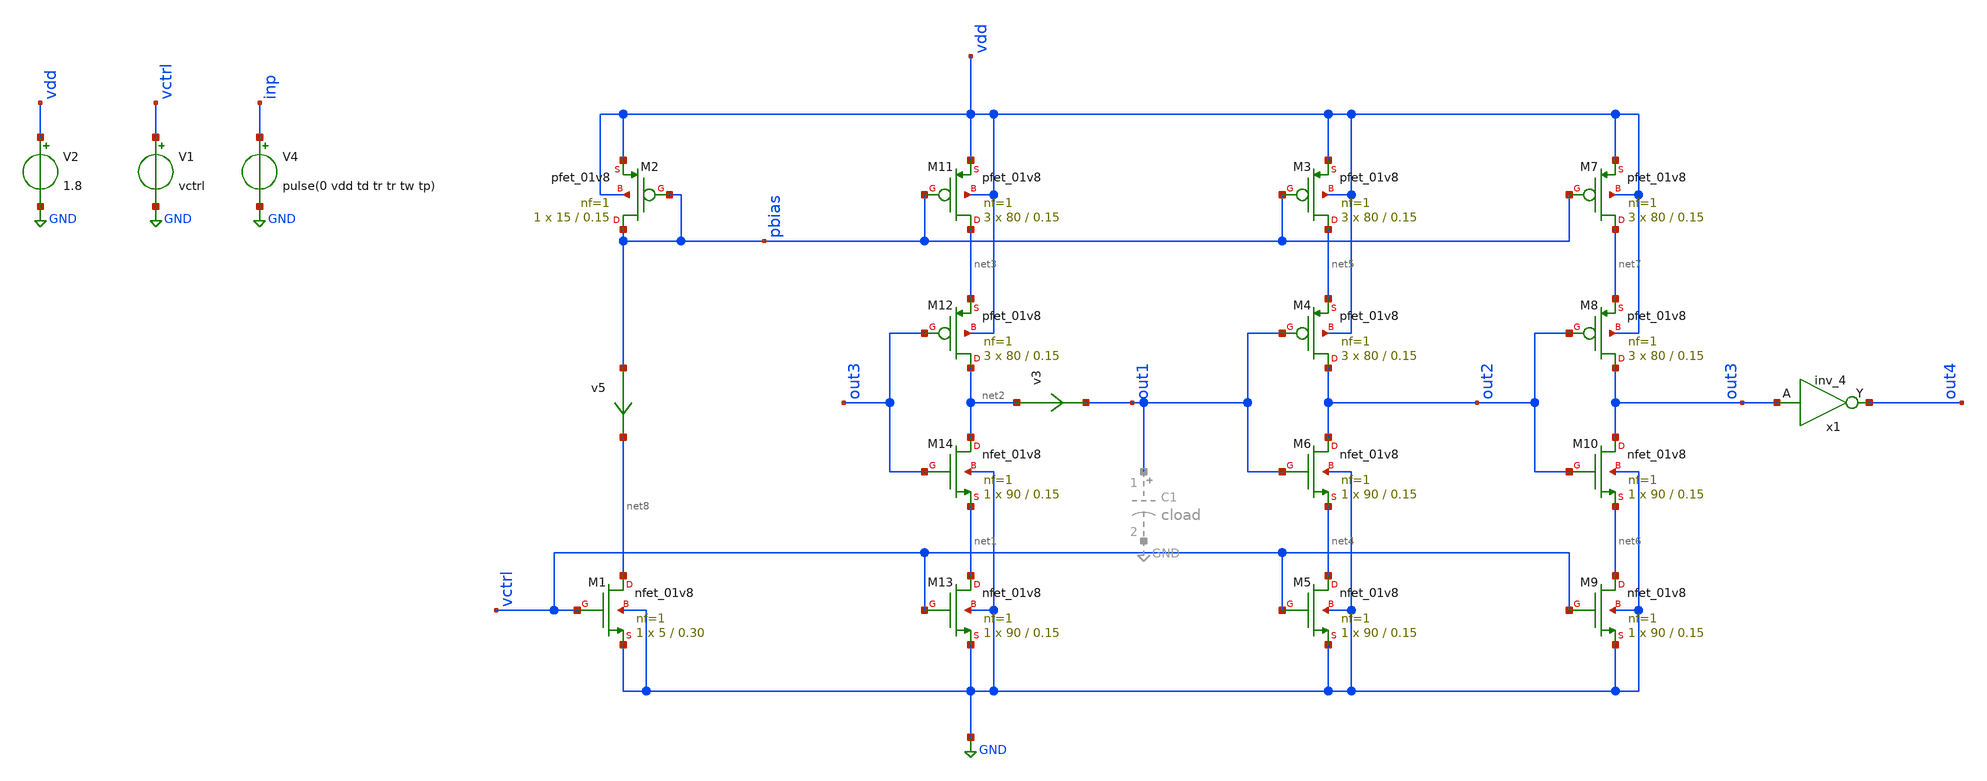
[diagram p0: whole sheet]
** sch_path: xschem/inv_delay.sch
**.subckt inv_delay
XM1 net8 vctrl GND GND sky130_fd_pr__nfet_01v8 L=0.30 W=5 nf=1 ad='int((nf+1)/2) * W/nf * 0.29' as='int((nf+2)/2) * W/nf * 0.29'
+ pd='2*int((nf+1)/2) * (W/nf + 0.29)' ps='2*int((nf+2)/2) * (W/nf + 0.29)' nrd='0.29 / W' nrs='0.29 / W'
+ sa=0 sb=0 sd=0 mult=1 m=1
XM2 pbias pbias vdd vdd sky130_fd_pr__pfet_01v8 L=0.15 W=15 nf=1 ad='int((nf+1)/2) * W/nf * 0.29' as='int((nf+2)/2) * W/nf * 0.29'
+ pd='2*int((nf+1)/2) * (W/nf + 0.29)' ps='2*int((nf+2)/2) * (W/nf + 0.29)' nrd='0.29 / W' nrs='0.29 / W'
+ sa=0 sb=0 sd=0 mult=1 m=1
XM11 net3 pbias vdd vdd sky130_fd_pr__pfet_01v8 L=0.15 W=80 nf=1 ad='int((nf+1)/2) * W/nf * 0.29' as='int((nf+2)/2) * W/nf * 0.29'
+ pd='2*int((nf+1)/2) * (W/nf + 0.29)' ps='2*int((nf+2)/2) * (W/nf + 0.29)' nrd='0.29 / W' nrs='0.29 / W'
+ sa=0 sb=0 sd=0 mult=3 m=3
XM12 net2 out3 net3 vdd sky130_fd_pr__pfet_01v8 L=0.15 W=80 nf=1 ad='int((nf+1)/2) * W/nf * 0.29' as='int((nf+2)/2) * W/nf * 0.29'
+ pd='2*int((nf+1)/2) * (W/nf + 0.29)' ps='2*int((nf+2)/2) * (W/nf + 0.29)' nrd='0.29 / W' nrs='0.29 / W'
+ sa=0 sb=0 sd=0 mult=3 m=3
XM13 net1 vctrl GND GND sky130_fd_pr__nfet_01v8 L=0.15 W=90 nf=1 ad='int((nf+1)/2) * W/nf * 0.29' as='int((nf+2)/2) * W/nf * 0.29'
+ pd='2*int((nf+1)/2) * (W/nf + 0.29)' ps='2*int((nf+2)/2) * (W/nf + 0.29)' nrd='0.29 / W' nrs='0.29 / W'
+ sa=0 sb=0 sd=0 mult=1 m=1
XM14 net2 out3 net1 GND sky130_fd_pr__nfet_01v8 L=0.15 W=90 nf=1 ad='int((nf+1)/2) * W/nf * 0.29' as='int((nf+2)/2) * W/nf * 0.29'
+ pd='2*int((nf+1)/2) * (W/nf + 0.29)' ps='2*int((nf+2)/2) * (W/nf + 0.29)' nrd='0.29 / W' nrs='0.29 / W'
+ sa=0 sb=0 sd=0 mult=1 m=1
V1 vctrl GND vctrl
V2 vdd GND 1.8
V4 inp GND pulse(0 vdd td tr tr tw tp)
XM3 net5 pbias vdd vdd sky130_fd_pr__pfet_01v8 L=0.15 W=80 nf=1 ad='int((nf+1)/2) * W/nf * 0.29' as='int((nf+2)/2) * W/nf * 0.29'
+ pd='2*int((nf+1)/2) * (W/nf + 0.29)' ps='2*int((nf+2)/2) * (W/nf + 0.29)' nrd='0.29 / W' nrs='0.29 / W'
+ sa=0 sb=0 sd=0 mult=3 m=3
XM4 out2 out1 net5 vdd sky130_fd_pr__pfet_01v8 L=0.15 W=80 nf=1 ad='int((nf+1)/2) * W/nf * 0.29' as='int((nf+2)/2) * W/nf * 0.29'
+ pd='2*int((nf+1)/2) * (W/nf + 0.29)' ps='2*int((nf+2)/2) * (W/nf + 0.29)' nrd='0.29 / W' nrs='0.29 / W'
+ sa=0 sb=0 sd=0 mult=3 m=3
XM5 net4 vctrl GND GND sky130_fd_pr__nfet_01v8 L=0.15 W=90 nf=1 ad='int((nf+1)/2) * W/nf * 0.29' as='int((nf+2)/2) * W/nf * 0.29'
+ pd='2*int((nf+1)/2) * (W/nf + 0.29)' ps='2*int((nf+2)/2) * (W/nf + 0.29)' nrd='0.29 / W' nrs='0.29 / W'
+ sa=0 sb=0 sd=0 mult=1 m=1
XM6 out2 out1 net4 GND sky130_fd_pr__nfet_01v8 L=0.15 W=90 nf=1 ad='int((nf+1)/2) * W/nf * 0.29' as='int((nf+2)/2) * W/nf * 0.29'
+ pd='2*int((nf+1)/2) * (W/nf + 0.29)' ps='2*int((nf+2)/2) * (W/nf + 0.29)' nrd='0.29 / W' nrs='0.29 / W'
+ sa=0 sb=0 sd=0 mult=1 m=1
XM7 net7 pbias vdd vdd sky130_fd_pr__pfet_01v8 L=0.15 W=80 nf=1 ad='int((nf+1)/2) * W/nf * 0.29' as='int((nf+2)/2) * W/nf * 0.29'
+ pd='2*int((nf+1)/2) * (W/nf + 0.29)' ps='2*int((nf+2)/2) * (W/nf + 0.29)' nrd='0.29 / W' nrs='0.29 / W'
+ sa=0 sb=0 sd=0 mult=3 m=3
XM8 out3 out2 net7 vdd sky130_fd_pr__pfet_01v8 L=0.15 W=80 nf=1 ad='int((nf+1)/2) * W/nf * 0.29' as='int((nf+2)/2) * W/nf * 0.29'
+ pd='2*int((nf+1)/2) * (W/nf + 0.29)' ps='2*int((nf+2)/2) * (W/nf + 0.29)' nrd='0.29 / W' nrs='0.29 / W'
+ sa=0 sb=0 sd=0 mult=3 m=3
XM9 net6 vctrl GND GND sky130_fd_pr__nfet_01v8 L=0.15 W=90 nf=1 ad='int((nf+1)/2) * W/nf * 0.29' as='int((nf+2)/2) * W/nf * 0.29'
+ pd='2*int((nf+1)/2) * (W/nf + 0.29)' ps='2*int((nf+2)/2) * (W/nf + 0.29)' nrd='0.29 / W' nrs='0.29 / W'
+ sa=0 sb=0 sd=0 mult=1 m=1
XM10 out3 out2 net6 GND sky130_fd_pr__nfet_01v8 L=0.15 W=90 nf=1 ad='int((nf+1)/2) * W/nf * 0.29' as='int((nf+2)/2) * W/nf * 0.29'
+ pd='2*int((nf+1)/2) * (W/nf + 0.29)' ps='2*int((nf+2)/2) * (W/nf + 0.29)' nrd='0.29 / W' nrs='0.29 / W'
+ sa=0 sb=0 sd=0 mult=1 m=1
x1 out3 GND GND VDD VDD out4 sky130_fd_sc_hd__inv_4
v3 net2 out1 0
.save i(v3)
v5 pbias net8 0
.save i(v5)
**** begin user architecture code

** opencircuitdesign pdks install
.lib $::SKYWATER_MODELS/sky130.lib.spice tt
.include $::SKYWATER_STDCELLS/sky130_fd_sc_hd.spice




.options acct list
.temp 25
.save all
.save @m.xm1.msky130_fd_pr__nfet_01v8[cgd]
.save @m.xm1.msky130_fd_pr__nfet_01v8[gm]

.param vctrl=0.8 vdd=1.8 cload=250f  td=20n tr=0.1n tw=10n  tp=20n

.control
op
write inv_delay.raw
set appendwrite

tran 0.001n 100n uic
meas tran tdelay01 TRIG v(out4) VAL=0.9 RISE=15 TARG v(out4) VAL=0.9 RISE=16
let fosc1= 1/tdelay01
print fosc1
save fosc1
remzerovec
write inv_delay.raw

.endc


**** end user architecture code
**.ends
.GLOBAL GND
.end
